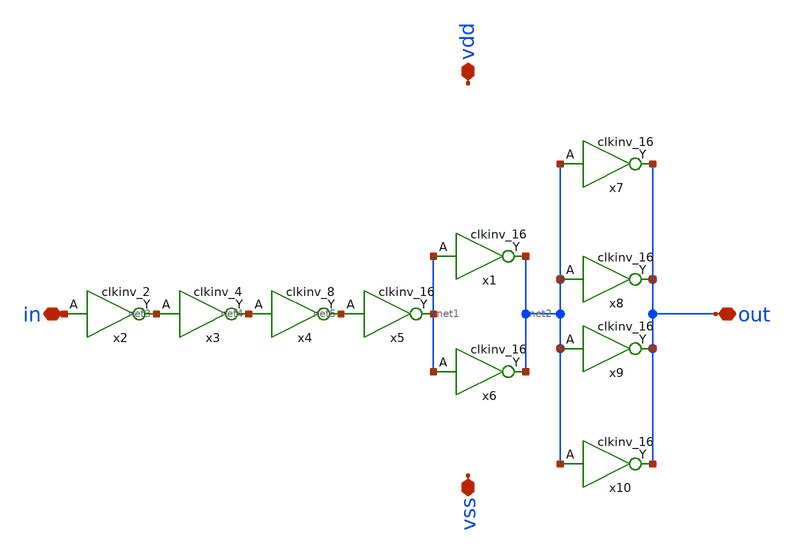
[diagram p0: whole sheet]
** sch_path: xschem/out_buf.sch
**.subckt out_buf out in vdd vss
*.iopin out
*.iopin in
*.iopin vdd
*.iopin vss
x2 in vss vss vdd vdd net3 sky130_fd_sc_hd__clkinv_2
x3 net3 vss vss vdd vdd net4 sky130_fd_sc_hd__clkinv_4
x4 net4 vss vss vdd vdd net5 sky130_fd_sc_hd__clkinv_8
x5 net5 vss vss vdd vdd net1 sky130_fd_sc_hd__clkinv_16
x1 net1 vss vss vdd vdd net2 sky130_fd_sc_hd__clkinv_16
x6 net1 vss vss vdd vdd net2 sky130_fd_sc_hd__clkinv_16
x7 net2 vss vss vdd vdd out sky130_fd_sc_hd__clkinv_16
x8 net2 vss vss vdd vdd out sky130_fd_sc_hd__clkinv_16
x9 net2 vss vss vdd vdd out sky130_fd_sc_hd__clkinv_16
x10 net2 vss vss vdd vdd out sky130_fd_sc_hd__clkinv_16
**.ends
.end
